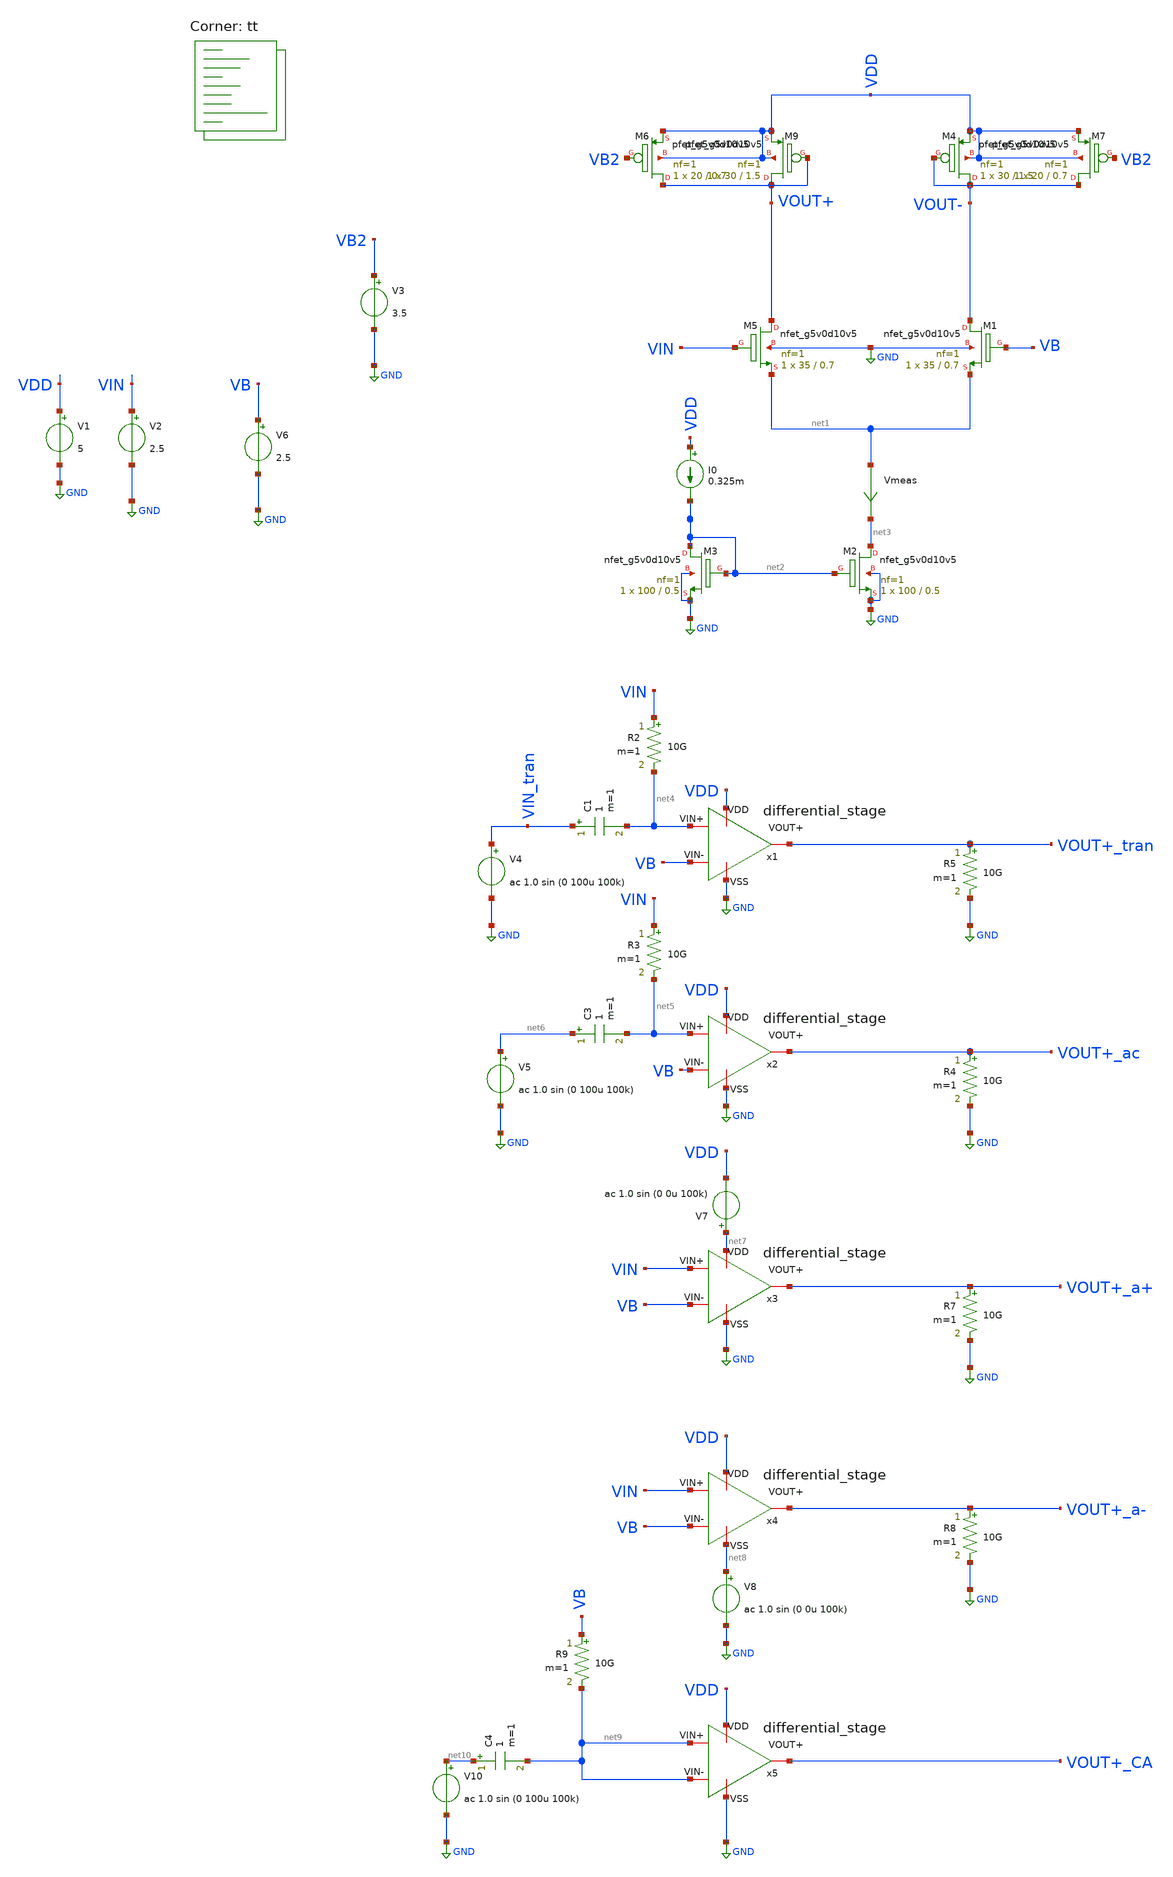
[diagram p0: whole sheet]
** sch_path: old stuff/amplifiers/differencial_stage_amps/stange stages/dual_load/diferential_stage.sch
**.subckt diferential_stage
XM5 VOUT+ VIN net1 GND sky130_fd_pr__nfet_g5v0d10v5 L=0.7 W=35 nf=1 ad='int((1 + 1)/2) * 35 / 1 * 0.29'
+ as='int((1 + 2)/2) * 35 / 1 * 0.29' pd='2*int((1 + 1)/2) * (35 / 1 + 0.29)' ps='2*int((1 + 2)/2) * (35 / 1 + 0.29)'
+ nrd='0.29 / 35 ' nrs='0.29 / 35 ' sa=0 sb=0 sd=0 mult=1 m=1
XM1 VOUT- VB net1 GND sky130_fd_pr__nfet_g5v0d10v5 L=0.7 W=35 nf=1 ad='int((1 + 1)/2) * 35 / 1 * 0.29'
+ as='int((1 + 2)/2) * 35 / 1 * 0.29' pd='2*int((1 + 1)/2) * (35 / 1 + 0.29)' ps='2*int((1 + 2)/2) * (35 / 1 + 0.29)'
+ nrd='0.29 / 35 ' nrs='0.29 / 35 ' sa=0 sb=0 sd=0 mult=1 m=1
V1 VDD GND 5
V2 VIN GND 2.5
V6 VB GND 2.5
XM2 net3 net2 GND GND sky130_fd_pr__nfet_g5v0d10v5 L=0.5 W=100 nf=1 ad='int((1 + 1)/2) * 100 / 1 * 0.29'
+ as='int((1 + 2)/2) * 100 / 1 * 0.29' pd='2*int((1 + 1)/2) * (100 / 1 + 0.29)' ps='2*int((1 + 2)/2) * (100 / 1 + 0.29)'
+ nrd='0.29 / 100 ' nrs='0.29 / 100 ' sa=0 sb=0 sd=0 mult=1 m=1
Vmeas net1 net3 0
.save i(vmeas)
R5 VOUT+_tran GND 10G m=1
R2 VIN net4 10G m=1
V4 VIN_tran GND ac 1.0 sin (0 100u 100k)
C1 VIN_tran net4 1 m=1
R3 VIN net5 10G m=1
C3 net6 net5 1 m=1
V5 net6 GND ac 1.0 sin (0 100u 100k)
R4 VOUT+_ac GND 10G m=1
V7 net7 VDD ac 1.0 sin (0 0u 100k)
R7 VOUT+_a+ GND 10G m=1
V8 net8 GND ac 1.0 sin (0 0u 100k)
R8 VOUT+_a- GND 10G m=1
R9 VB net9 10G m=1
C4 net10 net9 1 m=1
V10 net10 GND ac 1.0 sin (0 100u 100k)
XM3 net2 net2 GND GND sky130_fd_pr__nfet_g5v0d10v5 L=0.5 W=100 nf=1 ad='int((1 + 1)/2) * 100 / 1 * 0.29'
+ as='int((1 + 2)/2) * 100 / 1 * 0.29' pd='2*int((1 + 1)/2) * (100 / 1 + 0.29)' ps='2*int((1 + 2)/2) * (100 / 1 + 0.29)'
+ nrd='0.29 / 100 ' nrs='0.29 / 100 ' sa=0 sb=0 sd=0 mult=1 m=1
I0 VDD net2 0.325m
XM9 VOUT+ VOUT+ VDD VDD sky130_fd_pr__pfet_g5v0d10v5 L=1.5 W=30 nf=1 ad='int((1 + 1)/2) * 30 / 1 * 0.29'
+ as='int((1 + 2)/2) * 30 / 1 * 0.29' pd='2*int((1 + 1)/2) * (30 / 1 + 0.29)' ps='2*int((1 + 2)/2) * (30 / 1 + 0.29)'
+ nrd='0.29 / 30 ' nrs='0.29 / 30 ' sa=0 sb=0 sd=0 mult=1 m=1
XM4 VOUT- VOUT- VDD VDD sky130_fd_pr__pfet_g5v0d10v5 L=1.5 W=30 nf=1 ad='int((1 + 1)/2) * 30 / 1 * 0.29'
+ as='int((1 + 2)/2) * 30 / 1 * 0.29' pd='2*int((1 + 1)/2) * (30 / 1 + 0.29)' ps='2*int((1 + 2)/2) * (30 / 1 + 0.29)'
+ nrd='0.29 / 30 ' nrs='0.29 / 30 ' sa=0 sb=0 sd=0 mult=1 m=1
XM6 VOUT+ VB2 VDD VDD sky130_fd_pr__pfet_g5v0d10v5 L=0.7 W=20 nf=1 ad='int((1 + 1)/2) * 20 / 1 * 0.29'
+ as='int((1 + 2)/2) * 20 / 1 * 0.29' pd='2*int((1 + 1)/2) * (20 / 1 + 0.29)' ps='2*int((1 + 2)/2) * (20 / 1 + 0.29)'
+ nrd='0.29 / 20 ' nrs='0.29 / 20 ' sa=0 sb=0 sd=0 mult=1 m=1
XM7 VOUT- VB2 VDD VDD sky130_fd_pr__pfet_g5v0d10v5 L=0.7 W=20 nf=1 ad='int((1 + 1)/2) * 20 / 1 * 0.29'
+ as='int((1 + 2)/2) * 20 / 1 * 0.29' pd='2*int((1 + 1)/2) * (20 / 1 + 0.29)' ps='2*int((1 + 2)/2) * (20 / 1 + 0.29)'
+ nrd='0.29 / 20 ' nrs='0.29 / 20 ' sa=0 sb=0 sd=0 mult=1 m=1
V3 VB2 GND 3.5
x1 VDD GND net4 VB VOUT+_tran differential_stage
x2 VDD GND net5 VB VOUT+_ac differential_stage
x3 net7 GND VIN VB VOUT+_a+ differential_stage
x4 VDD net8 VIN VB VOUT+_a- differential_stage
x5 VDD GND net9 net9 VOUT+_CA differential_stage
**** begin user architecture code

**************************************************************
**************************************************************
**************************************************************
**************************************************************
**************************************************************
*LIBs*********************************************************
**************************************************************
**************************************************************
**************************************************************
**************************************************************
**************************************************************
*.lib $::SKYWATER_MODELS/sky130.lib.spice tt
* chose the corners in the corner file
* tt_mm for mismatch
* ss ff sf fs standart corners
* ll hh lh hl capacitor and resistors corners
* mc for total process variation including corners
**************************************************************
**************************************************************
**************************************************************
**************************************************************
**************************************************************
*Corners/montecarlo options***********************************
**************************************************************
**************************************************************
**************************************************************
**************************************************************
**************************************************************
.TEMP 27
**************************************************************
**************************************************************
**************************************************************
**************************************************************
*SIMULATION and Plots*****************************************
**************************************************************
**************************************************************
**************************************************************
**************************************************************
.control
save all
dc V2 0 5 0.01
*dc simulation
plot v(VOUT-) v(VIN) deriv(v(VOUT-)) v(VOUT+) deriv(v(VOUT+))
*ploting VIN VOUT and the voltage gain
plot i(Vmeas)
*ploting the current for curiosity
tran 1ns 20u
*transient simulation
plot (v(VOUT+_tran))
*simple plot to exemplify the gain
fft v(VOUT+_tran) v(VIN_tran)
*fast fourier transfor
plot mag(v(VOUT+_tran)) mag(v(VIN_tran))
ac dec 20 1 1000G
*simple ac simulation
plot db(v(VOUT+_ac))
plot db(v(VOUT+_a+))
plot db(v(VOUT+_a-))
plot db(v(VOUT+_CA))
plot db((v(VOUT+_ac))/(v(VOUT+_CA)))
plot db((v(VOUT+_ac))/(v(VOUT+_a+)))
plot db((v(VOUT+_ac))/(v(VOUT+_a-)))
.endc

.lib $::SKYWATER_MODELS/sky130.lib.spice tt
**** end user architecture code
**.ends
.GLOBAL GND
.end
